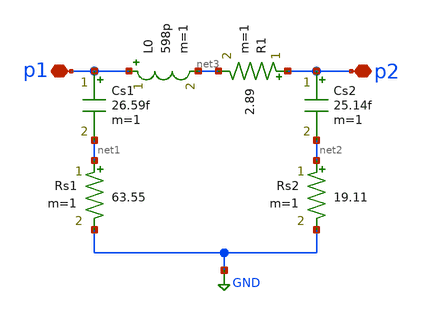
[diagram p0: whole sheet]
** sch_path: impedance-transformer/xschem/l1.sch
**.subckt l1 p2 p1
*.iopin p2
*.iopin p1
L0 p1 net3 598p m=1
Cs1 p1 net1 26.59f m=1
Cs2 p2 net2 25.14f m=1
Rs1 net1 GND 63.55 m=1
Rs2 net2 GND 19.11 m=1
R1 p2 net3 2.89 m=1
**.ends
.GLOBAL GND
.end
